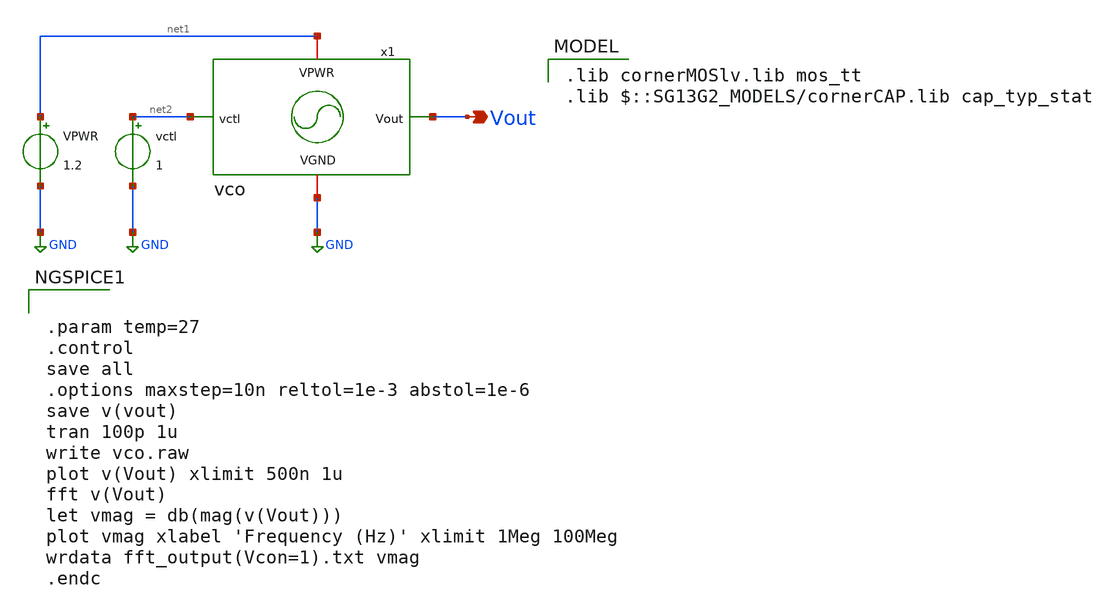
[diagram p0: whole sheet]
** sch_path: design_data/xschem/vco_pex_tb.sch
**.subckt vco_pex_tb Vout
*.opin Vout
VPWR net1 GND 1.2
vctl net2 GND 1
x1 net1 GND net2 Vout vco
**** begin user architecture code
 .lib cornerMOSlv.lib mos_tt
.lib $::SG13G2_MODELS/cornerCAP.lib cap_typ_stat



.param temp=27
.control
save all
.options maxstep=10n reltol=1e-3 abstol=1e-6
save v(vout)
tran 100p 1u
write vco.raw
plot v(Vout) xlimit 500n 1u
fft v(Vout)
let vmag = db(mag(v(Vout)))
plot vmag xlabel 'Frequency (Hz)' xlimit 1Meg 100Meg
wrdata fft_output(Vcon=1).txt vmag
.endc


**** end user architecture code
**.ends
.GLOBAL GND
.end
